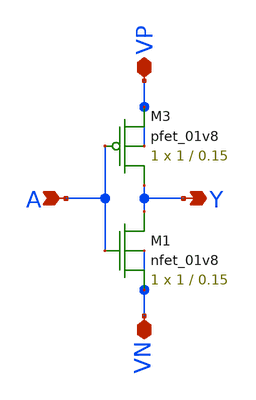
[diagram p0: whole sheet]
** sch_path: MP2/inv.sch
**.subckt inv A Y VN VP
*.ipin A
*.opin Y
*.iopin VN
*.iopin VP
XM3 Y A VP VP sky130_fd_pr__pfet_01v8 L=0.15 W=1 nf=1 ad='int((nf+1)/2) * W/nf * 0.29' as='int((nf+2)/2) * W/nf * 0.29'
+ pd='2*int((nf+1)/2) * (W/nf + 0.29)' ps='2*int((nf+2)/2) * (W/nf + 0.29)' nrd='0.29 / W' nrs='0.29 / W'
+ sa=0 sb=0 sd=0 mult=1 m=1
XM1 Y A VN VN sky130_fd_pr__nfet_01v8 L=0.15 W=1 nf=1 ad='int((nf+1)/2) * W/nf * 0.29' as='int((nf+2)/2) * W/nf * 0.29'
+ pd='2*int((nf+1)/2) * (W/nf + 0.29)' ps='2*int((nf+2)/2) * (W/nf + 0.29)' nrd='0.29 / W' nrs='0.29 / W'
+ sa=0 sb=0 sd=0 mult=1 m=1
**** begin user architecture code





**** end user architecture code
**.ends
.end
